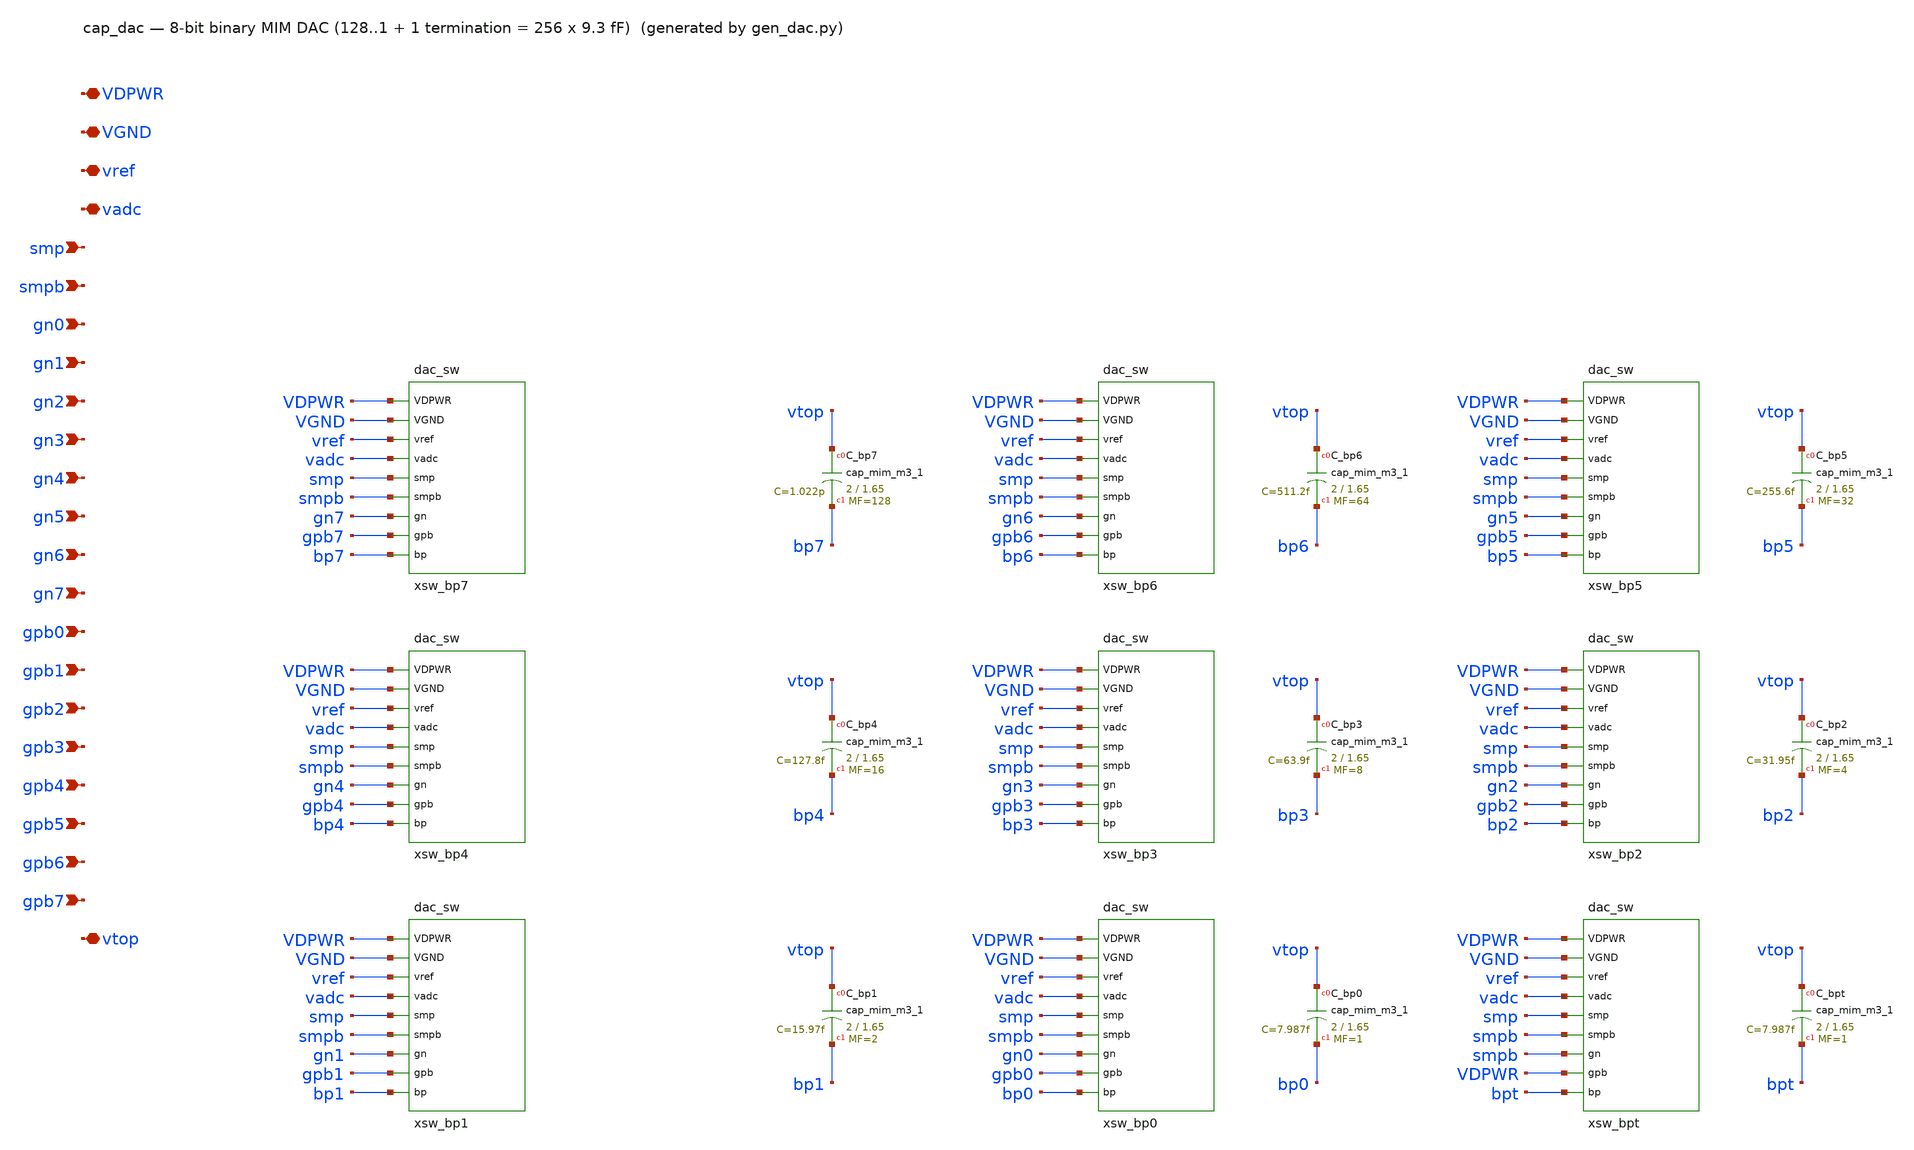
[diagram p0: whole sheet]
** sch_path: xschem/cap_dac.sch
**.subckt cap_dac VDPWR VGND vref vadc smp smpb gn0 gn1 gn2 gn3 gn4 gn5 gn6 gn7 gpb0 gpb1 gpb2 gpb3
*+ gpb4 gpb5 gpb6 gpb7 vtop
*.iopin VDPWR
*.iopin VGND
*.iopin vref
*.iopin vadc
*.ipin smp
*.ipin smpb
*.ipin gn0
*.ipin gn1
*.ipin gn2
*.ipin gn3
*.ipin gn4
*.ipin gn5
*.ipin gn6
*.ipin gn7
*.ipin gpb0
*.ipin gpb1
*.ipin gpb2
*.ipin gpb3
*.ipin gpb4
*.ipin gpb5
*.ipin gpb6
*.ipin gpb7
*.iopin vtop
xsw_bp7 VDPWR VGND vref vadc smp smpb gn7 gpb7 bp7 dac_sw
XC_bp7 vtop bp7 sky130_fd_pr__cap_mim_m3_1 W=2 L=1.65 MF=128 m=128
xsw_bp6 VDPWR VGND vref vadc smp smpb gn6 gpb6 bp6 dac_sw
XC_bp6 vtop bp6 sky130_fd_pr__cap_mim_m3_1 W=2 L=1.65 MF=64 m=64
xsw_bp5 VDPWR VGND vref vadc smp smpb gn5 gpb5 bp5 dac_sw
XC_bp5 vtop bp5 sky130_fd_pr__cap_mim_m3_1 W=2 L=1.65 MF=32 m=32
xsw_bp4 VDPWR VGND vref vadc smp smpb gn4 gpb4 bp4 dac_sw
XC_bp4 vtop bp4 sky130_fd_pr__cap_mim_m3_1 W=2 L=1.65 MF=16 m=16
xsw_bp3 VDPWR VGND vref vadc smp smpb gn3 gpb3 bp3 dac_sw
XC_bp3 vtop bp3 sky130_fd_pr__cap_mim_m3_1 W=2 L=1.65 MF=8 m=8
xsw_bp2 VDPWR VGND vref vadc smp smpb gn2 gpb2 bp2 dac_sw
XC_bp2 vtop bp2 sky130_fd_pr__cap_mim_m3_1 W=2 L=1.65 MF=4 m=4
xsw_bp1 VDPWR VGND vref vadc smp smpb gn1 gpb1 bp1 dac_sw
XC_bp1 vtop bp1 sky130_fd_pr__cap_mim_m3_1 W=2 L=1.65 MF=2 m=2
xsw_bp0 VDPWR VGND vref vadc smp smpb gn0 gpb0 bp0 dac_sw
XC_bp0 vtop bp0 sky130_fd_pr__cap_mim_m3_1 W=2 L=1.65 MF=1 m=1
xsw_bpt VDPWR VGND vref vadc smp smpb smpb VDPWR bpt dac_sw
XC_bpt vtop bpt sky130_fd_pr__cap_mim_m3_1 W=2 L=1.65 MF=1 m=1
**.ends

* expanding   symbol:  dac_sw.sym # of pins=9
** sym_path: xschem/dac_sw.sym
** sch_path: xschem/dac_sw.sch
.subckt dac_sw VDPWR VGND vref vadc smp smpb gn gpb bp
*.iopin VDPWR
*.iopin VGND
*.iopin vref
*.iopin vadc
*.ipin smp
*.ipin smpb
*.ipin gn
*.ipin gpb
*.iopin bp
XMSG bp gn VGND VGND sky130_fd_pr__nfet_01v8 L=0.15 W=1 nf=1 ad='int((1 + 1)/2) * 1 / 1 * 0.29' as='int((1 + 2)/2) * 1 / 1 * 0.29'
+ pd='2*int((1 + 1)/2) * (1 / 1 + 0.29)' ps='2*int((1 + 2)/2) * (1 / 1 + 0.29)' nrd='0.29 / 1 ' nrs='0.29 / 1 '
+ sa=0 sb=0 sd=0 mult=1 m=1
XMSR bp gpb vref VDPWR sky130_fd_pr__pfet_01v8_lvt L=0.35 W=4 nf=1 ad='int((1 + 1)/2) * 4 / 1 * 0.29'
+ as='int((1 + 2)/2) * 4 / 1 * 0.29' pd='2*int((1 + 1)/2) * (4 / 1 + 0.29)' ps='2*int((1 + 2)/2) * (4 / 1 + 0.29)'
+ nrd='0.29 / 4 ' nrs='0.29 / 4 ' sa=0 sb=0 sd=0 mult=1 m=1
XMSN bp smp vadc VGND sky130_fd_pr__nfet_01v8 L=0.15 W=1 nf=1 ad='int((1 + 1)/2) * 1 / 1 * 0.29' as='int((1 + 2)/2) * 1 / 1 * 0.29'
+ pd='2*int((1 + 1)/2) * (1 / 1 + 0.29)' ps='2*int((1 + 2)/2) * (1 / 1 + 0.29)' nrd='0.29 / 1 ' nrs='0.29 / 1 '
+ sa=0 sb=0 sd=0 mult=1 m=1
XMSP bp smpb vadc VDPWR sky130_fd_pr__pfet_01v8_lvt L=0.35 W=2 nf=1 ad='int((1 + 1)/2) * 2 / 1 * 0.29'
+ as='int((1 + 2)/2) * 2 / 1 * 0.29' pd='2*int((1 + 1)/2) * (2 / 1 + 0.29)' ps='2*int((1 + 2)/2) * (2 / 1 + 0.29)'
+ nrd='0.29 / 2 ' nrs='0.29 / 2 ' sa=0 sb=0 sd=0 mult=1 m=1
.ends

.end
